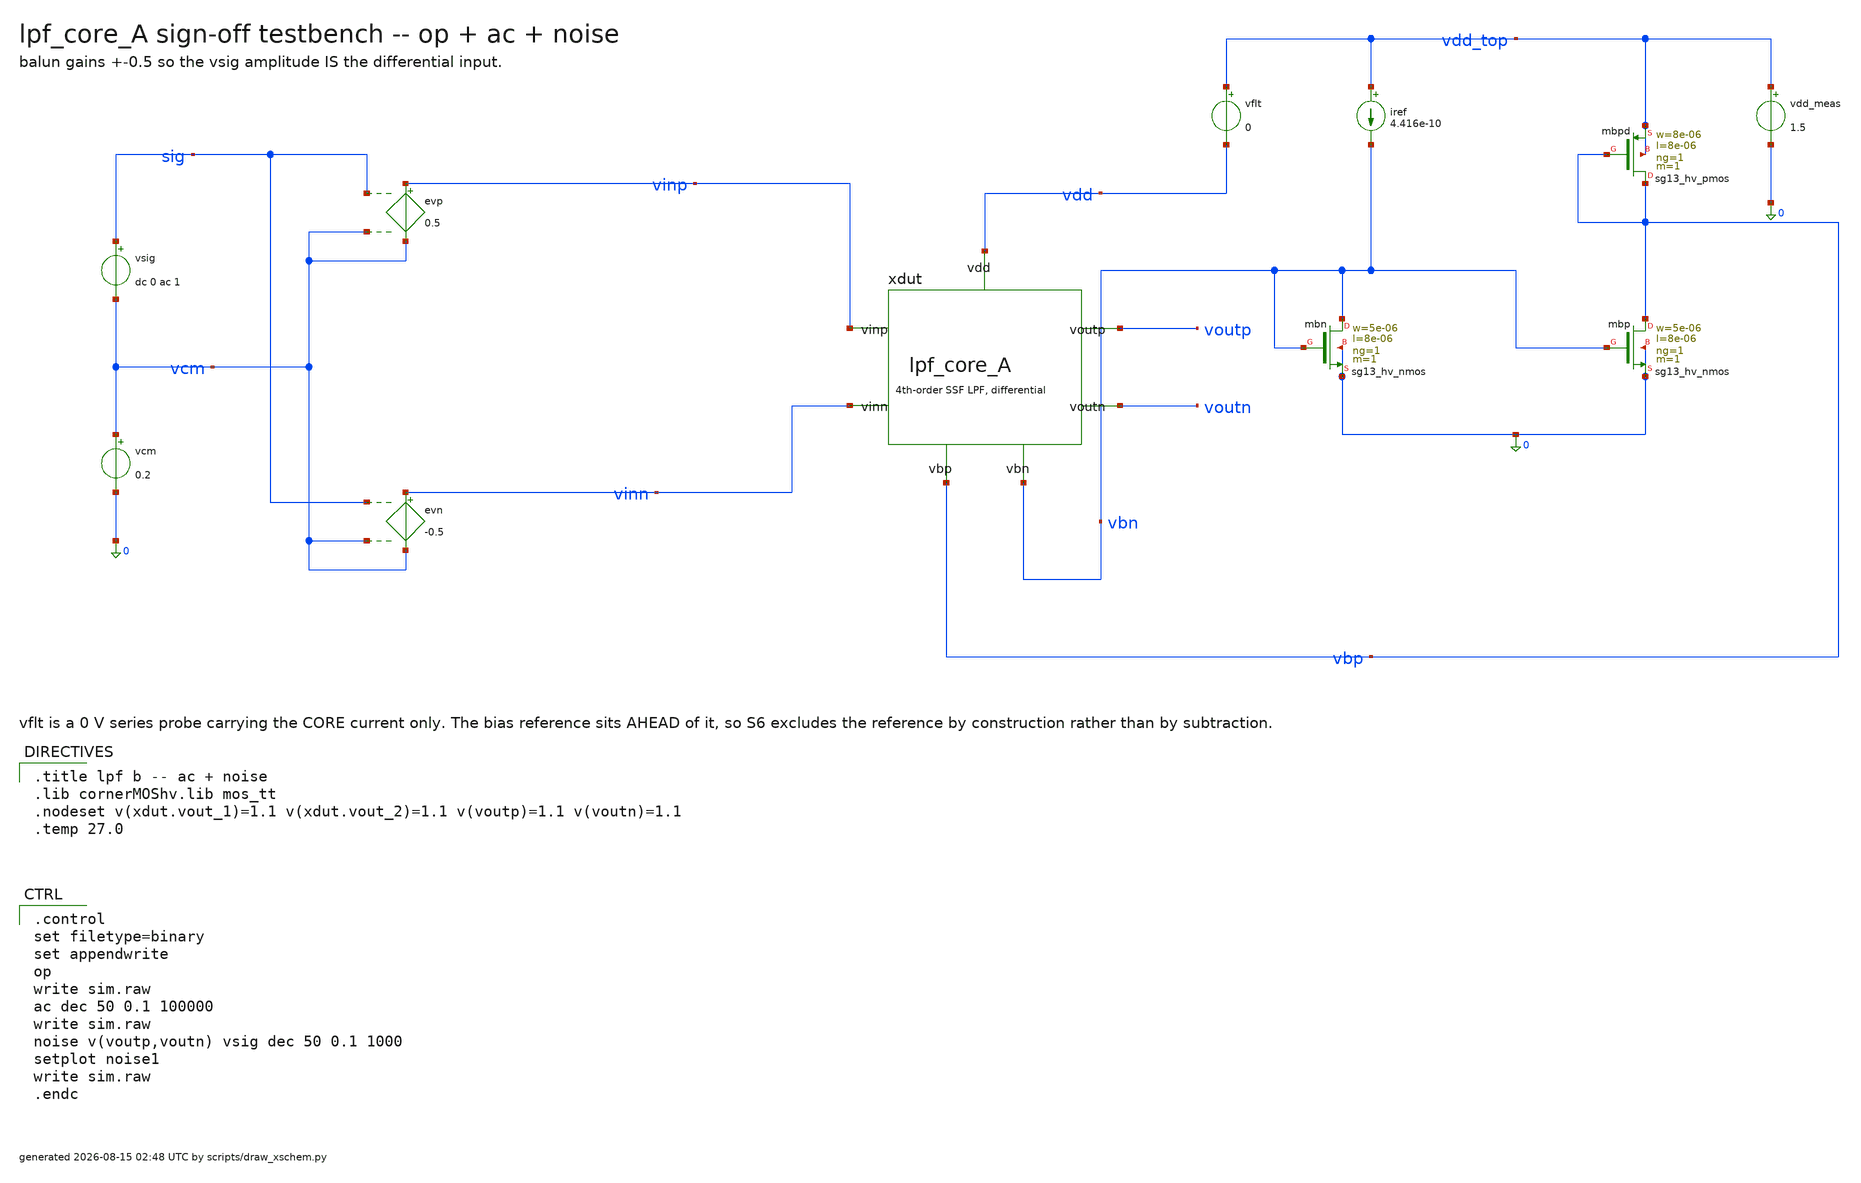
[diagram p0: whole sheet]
** sch_path: signoff/A-minarea/lpf_tb_A.sch
**.subckt lpf_tb_A
vsig sig vcm dc 0 ac 1
vcm vcm 0 0.2
evp vinp vcm sig vcm 0.5
evn vinn vcm sig vcm -0.5
xdut vinp vinn voutp voutn vbn vbp vdd lpf_core_A
vflt vdd_top vdd 0
vdd_meas vdd_top 0 1.5
iref vdd_top vbn 4.416e-10
Xmbn vbn vbn 0 0 sg13_hv_nmos w=5e-06 l=8e-06 ng=1 m=1 mm_ok=1
Xmbp vbp vbn 0 0 sg13_hv_nmos w=5e-06 l=8e-06 ng=1 m=1 mm_ok=1
Xmbpd vbp vbp vdd_top vdd_top sg13_hv_pmos w=8e-06 l=8e-06 ng=1 m=1 mm_ok=1
**** begin user architecture code

.title lpf b -- ac + noise
.lib cornerMOShv.lib mos_tt
.nodeset v(xdut.vout_1)=1.1 v(xdut.vout_2)=1.1 v(voutp)=1.1 v(voutn)=1.1
.temp 27.0


.control
set filetype=binary
set appendwrite
op
write sim.raw
ac dec 50 0.1 100000
write sim.raw
noise v(voutp,voutn) vsig dec 50 0.1 1000
setplot noise1
write sim.raw
.endc

**** end user architecture code
**.ends
.end
